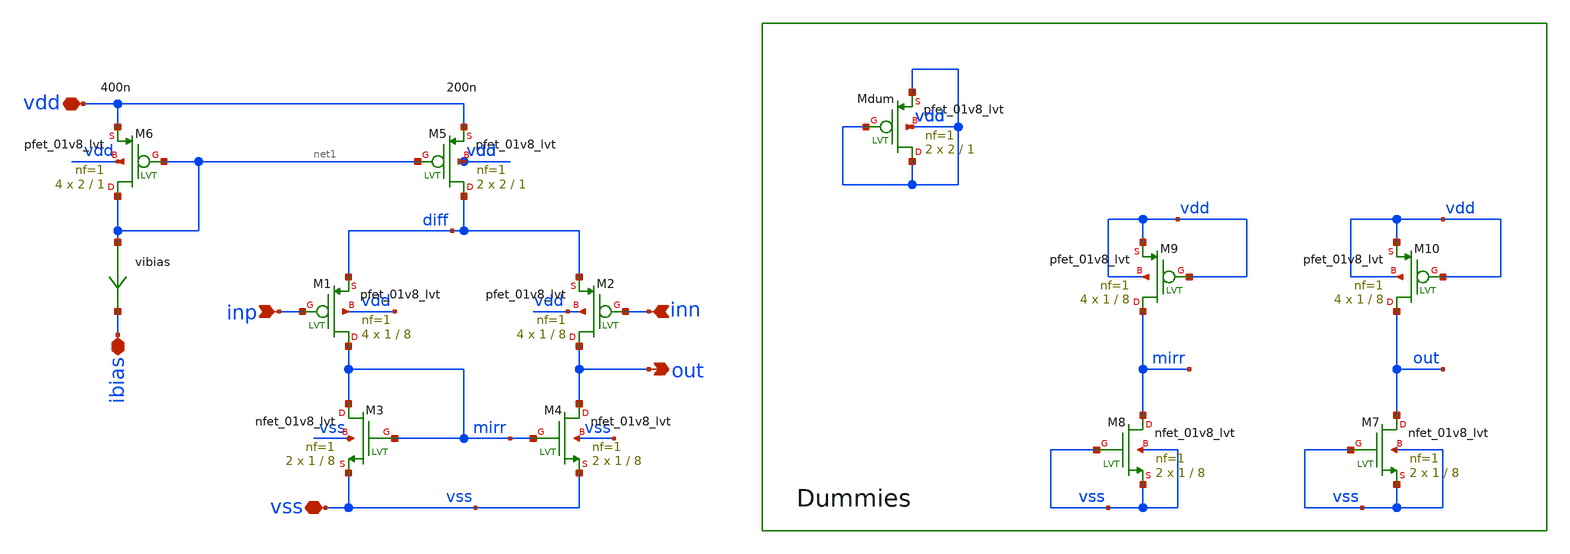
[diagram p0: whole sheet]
** sch_path: xschem/bandgap/bandgap_amp.sch
**.subckt bandgap_amp out inp inn vdd vss ibias
*.opin out
*.ipin inp
*.ipin inn
*.iopin vdd
*.iopin vss
*.iopin ibias
vibias net1 ibias 0
.save i(vibias)
XM4 out mirr vss vss sky130_fd_pr__nfet_01v8_lvt L=8 W=1 nf=1 ad='int((nf+1)/2) * W/nf * 0.29' as='int((nf+2)/2) * W/nf * 0.29'
+ pd='2*int((nf+1)/2) * (W/nf + 0.29)' ps='2*int((nf+2)/2) * (W/nf + 0.29)' nrd='0.29 / W' nrs='0.29 / W'
+ sa=0 sb=0 sd=0 mult=2 m=2
XM3 mirr mirr vss vss sky130_fd_pr__nfet_01v8_lvt L=8 W=1 nf=1 ad='int((nf+1)/2) * W/nf * 0.29' as='int((nf+2)/2) * W/nf * 0.29'
+ pd='2*int((nf+1)/2) * (W/nf + 0.29)' ps='2*int((nf+2)/2) * (W/nf + 0.29)' nrd='0.29 / W' nrs='0.29 / W'
+ sa=0 sb=0 sd=0 mult=2 m=2
XM1 mirr inp diff vdd sky130_fd_pr__pfet_01v8_lvt L=8 W=1 nf=1 ad='int((nf+1)/2) * W/nf * 0.29' as='int((nf+2)/2) * W/nf * 0.29'
+ pd='2*int((nf+1)/2) * (W/nf + 0.29)' ps='2*int((nf+2)/2) * (W/nf + 0.29)' nrd='0.29 / W' nrs='0.29 / W'
+ sa=0 sb=0 sd=0 mult=4 m=4
XM2 out inn diff vdd sky130_fd_pr__pfet_01v8_lvt L=8 W=1 nf=1 ad='int((nf+1)/2) * W/nf * 0.29' as='int((nf+2)/2) * W/nf * 0.29'
+ pd='2*int((nf+1)/2) * (W/nf + 0.29)' ps='2*int((nf+2)/2) * (W/nf + 0.29)' nrd='0.29 / W' nrs='0.29 / W'
+ sa=0 sb=0 sd=0 mult=4 m=4
XM5 diff net1 vdd vdd sky130_fd_pr__pfet_01v8_lvt L=1 W=2 nf=1 ad='int((nf+1)/2) * W/nf * 0.29' as='int((nf+2)/2) * W/nf * 0.29'
+ pd='2*int((nf+1)/2) * (W/nf + 0.29)' ps='2*int((nf+2)/2) * (W/nf + 0.29)' nrd='0.29 / W' nrs='0.29 / W'
+ sa=0 sb=0 sd=0 mult=2 m=2
XM6 net1 net1 vdd vdd sky130_fd_pr__pfet_01v8_lvt L=1 W=2 nf=1 ad='int((nf+1)/2) * W/nf * 0.29' as='int((nf+2)/2) * W/nf * 0.29'
+ pd='2*int((nf+1)/2) * (W/nf + 0.29)' ps='2*int((nf+2)/2) * (W/nf + 0.29)' nrd='0.29 / W' nrs='0.29 / W'
+ sa=0 sb=0 sd=0 mult=4 m=4
XMdum vdd vdd vdd vdd sky130_fd_pr__pfet_01v8_lvt L=1 W=2 nf=1 ad='int((nf+1)/2) * W/nf * 0.29' as='int((nf+2)/2) * W/nf * 0.29'
+ pd='2*int((nf+1)/2) * (W/nf + 0.29)' ps='2*int((nf+2)/2) * (W/nf + 0.29)' nrd='0.29 / W' nrs='0.29 / W'
+ sa=0 sb=0 sd=0 mult=2 m=2
XM7 out vss vss vss sky130_fd_pr__nfet_01v8_lvt L=8 W=1 nf=1 ad='int((nf+1)/2) * W/nf * 0.29' as='int((nf+2)/2) * W/nf * 0.29'
+ pd='2*int((nf+1)/2) * (W/nf + 0.29)' ps='2*int((nf+2)/2) * (W/nf + 0.29)' nrd='0.29 / W' nrs='0.29 / W'
+ sa=0 sb=0 sd=0 mult=2 m=2
XM8 mirr vss vss vss sky130_fd_pr__nfet_01v8_lvt L=8 W=1 nf=1 ad='int((nf+1)/2) * W/nf * 0.29' as='int((nf+2)/2) * W/nf * 0.29'
+ pd='2*int((nf+1)/2) * (W/nf + 0.29)' ps='2*int((nf+2)/2) * (W/nf + 0.29)' nrd='0.29 / W' nrs='0.29 / W'
+ sa=0 sb=0 sd=0 mult=2 m=2
XM9 mirr vdd vdd vdd sky130_fd_pr__pfet_01v8_lvt L=8 W=1 nf=1 ad='int((nf+1)/2) * W/nf * 0.29' as='int((nf+2)/2) * W/nf * 0.29'
+ pd='2*int((nf+1)/2) * (W/nf + 0.29)' ps='2*int((nf+2)/2) * (W/nf + 0.29)' nrd='0.29 / W' nrs='0.29 / W'
+ sa=0 sb=0 sd=0 mult=4 m=4
XM10 out vdd vdd vdd sky130_fd_pr__pfet_01v8_lvt L=8 W=1 nf=1 ad='int((nf+1)/2) * W/nf * 0.29' as='int((nf+2)/2) * W/nf * 0.29'
+ pd='2*int((nf+1)/2) * (W/nf + 0.29)' ps='2*int((nf+2)/2) * (W/nf + 0.29)' nrd='0.29 / W' nrs='0.29 / W'
+ sa=0 sb=0 sd=0 mult=4 m=4
**.ends
.end
